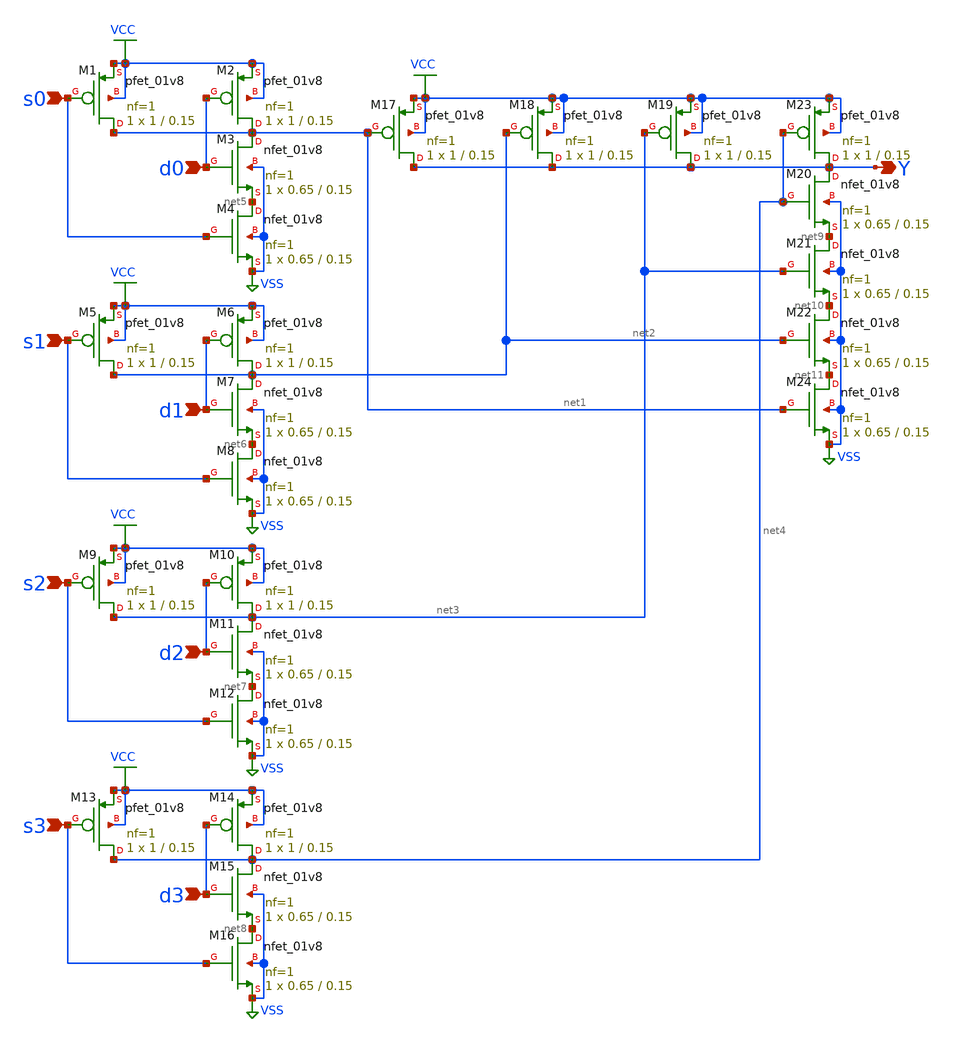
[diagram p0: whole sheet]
** sch_path: elements/mux4.sch
**.subckt mux4 s0 d0 s1 d1 s2 d2 s3 d3 Y
*.ipin s0
*.ipin d0
*.ipin s1
*.ipin d1
*.ipin s2
*.ipin d2
*.ipin s3
*.ipin d3
*.opin Y
XM1 net1 s0 VCC VCC sky130_fd_pr__pfet_01v8 L=0.15 W=1 nf=1 ad='int((nf+1)/2) * W/nf * 0.29' as='int((nf+2)/2) * W/nf * 0.29'
+ pd='2*int((nf+1)/2) * (W/nf + 0.29)' ps='2*int((nf+2)/2) * (W/nf + 0.29)' nrd='0.29 / W' nrs='0.29 / W'
+ sa=0 sb=0 sd=0 mult=1 m=1
XM2 net1 d0 VCC VCC sky130_fd_pr__pfet_01v8 L=0.15 W=1 nf=1 ad='int((nf+1)/2) * W/nf * 0.29' as='int((nf+2)/2) * W/nf * 0.29'
+ pd='2*int((nf+1)/2) * (W/nf + 0.29)' ps='2*int((nf+2)/2) * (W/nf + 0.29)' nrd='0.29 / W' nrs='0.29 / W'
+ sa=0 sb=0 sd=0 mult=1 m=1
XM3 net1 d0 net5 VSS sky130_fd_pr__nfet_01v8 L=0.15 W=0.65 nf=1 ad='int((1 + 1)/2) * 0.65 / 1 * 0.29'
+ as='int((1 + 2)/2) * 0.65 / 1 * 0.29' pd='2*int((1 + 1)/2) * (0.65 / 1 + 0.29)' ps='2*int((1 + 2)/2) * (0.65 / 1 + 0.29)'
+ nrd='0.29 / 0.65 ' nrs='0.29 / 0.65 ' sa=0 sb=0 sd=0 mult=1 m=1
XM4 net5 s0 VSS VSS sky130_fd_pr__nfet_01v8 L=0.15 W=0.65 nf=1 ad='int((1 + 1)/2) * 0.65 / 1 * 0.29'
+ as='int((1 + 2)/2) * 0.65 / 1 * 0.29' pd='2*int((1 + 1)/2) * (0.65 / 1 + 0.29)' ps='2*int((1 + 2)/2) * (0.65 / 1 + 0.29)'
+ nrd='0.29 / 0.65 ' nrs='0.29 / 0.65 ' sa=0 sb=0 sd=0 mult=1 m=1
XM5 net2 s1 VCC VCC sky130_fd_pr__pfet_01v8 L=0.15 W=1 nf=1 ad='int((nf+1)/2) * W/nf * 0.29' as='int((nf+2)/2) * W/nf * 0.29'
+ pd='2*int((nf+1)/2) * (W/nf + 0.29)' ps='2*int((nf+2)/2) * (W/nf + 0.29)' nrd='0.29 / W' nrs='0.29 / W'
+ sa=0 sb=0 sd=0 mult=1 m=1
XM6 net2 d1 VCC VCC sky130_fd_pr__pfet_01v8 L=0.15 W=1 nf=1 ad='int((nf+1)/2) * W/nf * 0.29' as='int((nf+2)/2) * W/nf * 0.29'
+ pd='2*int((nf+1)/2) * (W/nf + 0.29)' ps='2*int((nf+2)/2) * (W/nf + 0.29)' nrd='0.29 / W' nrs='0.29 / W'
+ sa=0 sb=0 sd=0 mult=1 m=1
XM7 net2 d1 net6 VSS sky130_fd_pr__nfet_01v8 L=0.15 W=0.65 nf=1 ad='int((1 + 1)/2) * 0.65 / 1 * 0.29'
+ as='int((1 + 2)/2) * 0.65 / 1 * 0.29' pd='2*int((1 + 1)/2) * (0.65 / 1 + 0.29)' ps='2*int((1 + 2)/2) * (0.65 / 1 + 0.29)'
+ nrd='0.29 / 0.65 ' nrs='0.29 / 0.65 ' sa=0 sb=0 sd=0 mult=1 m=1
XM8 net6 s1 VSS VSS sky130_fd_pr__nfet_01v8 L=0.15 W=0.65 nf=1 ad='int((1 + 1)/2) * 0.65 / 1 * 0.29'
+ as='int((1 + 2)/2) * 0.65 / 1 * 0.29' pd='2*int((1 + 1)/2) * (0.65 / 1 + 0.29)' ps='2*int((1 + 2)/2) * (0.65 / 1 + 0.29)'
+ nrd='0.29 / 0.65 ' nrs='0.29 / 0.65 ' sa=0 sb=0 sd=0 mult=1 m=1
XM9 net3 s2 VCC VCC sky130_fd_pr__pfet_01v8 L=0.15 W=1 nf=1 ad='int((nf+1)/2) * W/nf * 0.29' as='int((nf+2)/2) * W/nf * 0.29'
+ pd='2*int((nf+1)/2) * (W/nf + 0.29)' ps='2*int((nf+2)/2) * (W/nf + 0.29)' nrd='0.29 / W' nrs='0.29 / W'
+ sa=0 sb=0 sd=0 mult=1 m=1
XM10 net3 d2 VCC VCC sky130_fd_pr__pfet_01v8 L=0.15 W=1 nf=1 ad='int((nf+1)/2) * W/nf * 0.29' as='int((nf+2)/2) * W/nf * 0.29'
+ pd='2*int((nf+1)/2) * (W/nf + 0.29)' ps='2*int((nf+2)/2) * (W/nf + 0.29)' nrd='0.29 / W' nrs='0.29 / W'
+ sa=0 sb=0 sd=0 mult=1 m=1
XM11 net3 d2 net7 VSS sky130_fd_pr__nfet_01v8 L=0.15 W=0.65 nf=1 ad='int((1 + 1)/2) * 0.65 / 1 * 0.29'
+ as='int((1 + 2)/2) * 0.65 / 1 * 0.29' pd='2*int((1 + 1)/2) * (0.65 / 1 + 0.29)' ps='2*int((1 + 2)/2) * (0.65 / 1 + 0.29)'
+ nrd='0.29 / 0.65 ' nrs='0.29 / 0.65 ' sa=0 sb=0 sd=0 mult=1 m=1
XM12 net7 s2 VSS VSS sky130_fd_pr__nfet_01v8 L=0.15 W=0.65 nf=1 ad='int((1 + 1)/2) * 0.65 / 1 * 0.29'
+ as='int((1 + 2)/2) * 0.65 / 1 * 0.29' pd='2*int((1 + 1)/2) * (0.65 / 1 + 0.29)' ps='2*int((1 + 2)/2) * (0.65 / 1 + 0.29)'
+ nrd='0.29 / 0.65 ' nrs='0.29 / 0.65 ' sa=0 sb=0 sd=0 mult=1 m=1
XM13 net4 s3 VCC VCC sky130_fd_pr__pfet_01v8 L=0.15 W=1 nf=1 ad='int((nf+1)/2) * W/nf * 0.29' as='int((nf+2)/2) * W/nf * 0.29'
+ pd='2*int((nf+1)/2) * (W/nf + 0.29)' ps='2*int((nf+2)/2) * (W/nf + 0.29)' nrd='0.29 / W' nrs='0.29 / W'
+ sa=0 sb=0 sd=0 mult=1 m=1
XM14 net4 d3 VCC VCC sky130_fd_pr__pfet_01v8 L=0.15 W=1 nf=1 ad='int((nf+1)/2) * W/nf * 0.29' as='int((nf+2)/2) * W/nf * 0.29'
+ pd='2*int((nf+1)/2) * (W/nf + 0.29)' ps='2*int((nf+2)/2) * (W/nf + 0.29)' nrd='0.29 / W' nrs='0.29 / W'
+ sa=0 sb=0 sd=0 mult=1 m=1
XM15 net4 d3 net8 VSS sky130_fd_pr__nfet_01v8 L=0.15 W=0.65 nf=1 ad='int((1 + 1)/2) * 0.65 / 1 * 0.29'
+ as='int((1 + 2)/2) * 0.65 / 1 * 0.29' pd='2*int((1 + 1)/2) * (0.65 / 1 + 0.29)' ps='2*int((1 + 2)/2) * (0.65 / 1 + 0.29)'
+ nrd='0.29 / 0.65 ' nrs='0.29 / 0.65 ' sa=0 sb=0 sd=0 mult=1 m=1
XM16 net8 s3 VSS VSS sky130_fd_pr__nfet_01v8 L=0.15 W=0.65 nf=1 ad='int((1 + 1)/2) * 0.65 / 1 * 0.29'
+ as='int((1 + 2)/2) * 0.65 / 1 * 0.29' pd='2*int((1 + 1)/2) * (0.65 / 1 + 0.29)' ps='2*int((1 + 2)/2) * (0.65 / 1 + 0.29)'
+ nrd='0.29 / 0.65 ' nrs='0.29 / 0.65 ' sa=0 sb=0 sd=0 mult=1 m=1
XM17 Y net1 VCC VCC sky130_fd_pr__pfet_01v8 L=0.15 W=1 nf=1 ad='int((nf+1)/2) * W/nf * 0.29' as='int((nf+2)/2) * W/nf * 0.29'
+ pd='2*int((nf+1)/2) * (W/nf + 0.29)' ps='2*int((nf+2)/2) * (W/nf + 0.29)' nrd='0.29 / W' nrs='0.29 / W'
+ sa=0 sb=0 sd=0 mult=1 m=1
XM18 Y net2 VCC VCC sky130_fd_pr__pfet_01v8 L=0.15 W=1 nf=1 ad='int((nf+1)/2) * W/nf * 0.29' as='int((nf+2)/2) * W/nf * 0.29'
+ pd='2*int((nf+1)/2) * (W/nf + 0.29)' ps='2*int((nf+2)/2) * (W/nf + 0.29)' nrd='0.29 / W' nrs='0.29 / W'
+ sa=0 sb=0 sd=0 mult=1 m=1
XM19 Y net3 VCC VCC sky130_fd_pr__pfet_01v8 L=0.15 W=1 nf=1 ad='int((nf+1)/2) * W/nf * 0.29' as='int((nf+2)/2) * W/nf * 0.29'
+ pd='2*int((nf+1)/2) * (W/nf + 0.29)' ps='2*int((nf+2)/2) * (W/nf + 0.29)' nrd='0.29 / W' nrs='0.29 / W'
+ sa=0 sb=0 sd=0 mult=1 m=1
XM20 Y net4 net9 VSS sky130_fd_pr__nfet_01v8 L=0.15 W=0.65 nf=1 ad='int((1 + 1)/2) * 0.65 / 1 * 0.29'
+ as='int((1 + 2)/2) * 0.65 / 1 * 0.29' pd='2*int((1 + 1)/2) * (0.65 / 1 + 0.29)' ps='2*int((1 + 2)/2) * (0.65 / 1 + 0.29)'
+ nrd='0.29 / 0.65 ' nrs='0.29 / 0.65 ' sa=0 sb=0 sd=0 mult=1 m=1
XM21 net9 net3 net10 VSS sky130_fd_pr__nfet_01v8 L=0.15 W=0.65 nf=1 ad='int((1 + 1)/2) * 0.65 / 1 * 0.29'
+ as='int((1 + 2)/2) * 0.65 / 1 * 0.29' pd='2*int((1 + 1)/2) * (0.65 / 1 + 0.29)' ps='2*int((1 + 2)/2) * (0.65 / 1 + 0.29)'
+ nrd='0.29 / 0.65 ' nrs='0.29 / 0.65 ' sa=0 sb=0 sd=0 mult=1 m=1
XM22 net10 net2 net11 VSS sky130_fd_pr__nfet_01v8 L=0.15 W=0.65 nf=1 ad='int((1 + 1)/2) * 0.65 / 1 * 0.29'
+ as='int((1 + 2)/2) * 0.65 / 1 * 0.29' pd='2*int((1 + 1)/2) * (0.65 / 1 + 0.29)' ps='2*int((1 + 2)/2) * (0.65 / 1 + 0.29)'
+ nrd='0.29 / 0.65 ' nrs='0.29 / 0.65 ' sa=0 sb=0 sd=0 mult=1 m=1
XM23 Y net4 VCC VCC sky130_fd_pr__pfet_01v8 L=0.15 W=1 nf=1 ad='int((nf+1)/2) * W/nf * 0.29' as='int((nf+2)/2) * W/nf * 0.29'
+ pd='2*int((nf+1)/2) * (W/nf + 0.29)' ps='2*int((nf+2)/2) * (W/nf + 0.29)' nrd='0.29 / W' nrs='0.29 / W'
+ sa=0 sb=0 sd=0 mult=1 m=1
XM24 net11 net1 VSS VSS sky130_fd_pr__nfet_01v8 L=0.15 W=0.65 nf=1 ad='int((1 + 1)/2) * 0.65 / 1 * 0.29'
+ as='int((1 + 2)/2) * 0.65 / 1 * 0.29' pd='2*int((1 + 1)/2) * (0.65 / 1 + 0.29)' ps='2*int((1 + 2)/2) * (0.65 / 1 + 0.29)'
+ nrd='0.29 / 0.65 ' nrs='0.29 / 0.65 ' sa=0 sb=0 sd=0 mult=1 m=1
**.ends
.GLOBAL VCC
.GLOBAL VSS
.end
